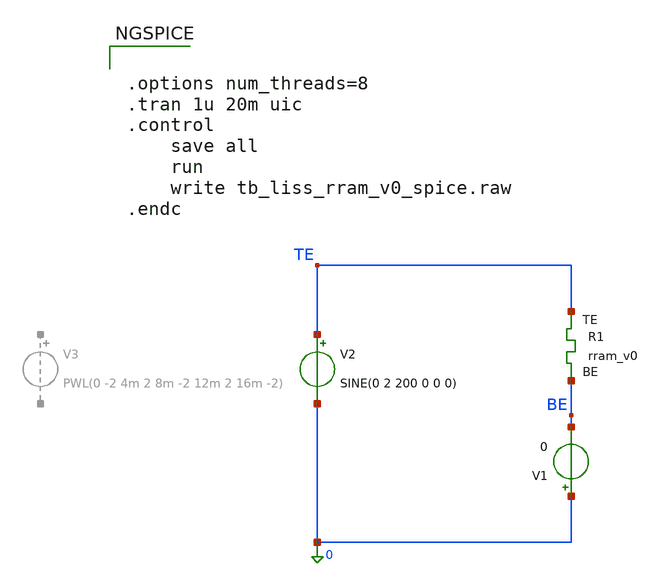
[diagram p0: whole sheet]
** sch_path: memristor_models/wellposed_spice/tb_liss_rram_v0_spice.sch
**.subckt tb_liss_rram_v0_spice
XR1 TE BE rram_v0
V2 TE 0 SINE(0 2 200 0 0 0)
V1 0 BE 0
**** begin user architecture code


.options num_threads=8
.tran 1u 20m uic
.control
	save all
	run
	write tb_liss_rram_v0_spice.raw
.endc




** opencircuitdesign pdks install
.inc /home/alex/Desktop/EDA/SNN_IPN/memristor_models/wellposed_spice/wllpsd.spice

**** end user architecture code
**.ends
.end
